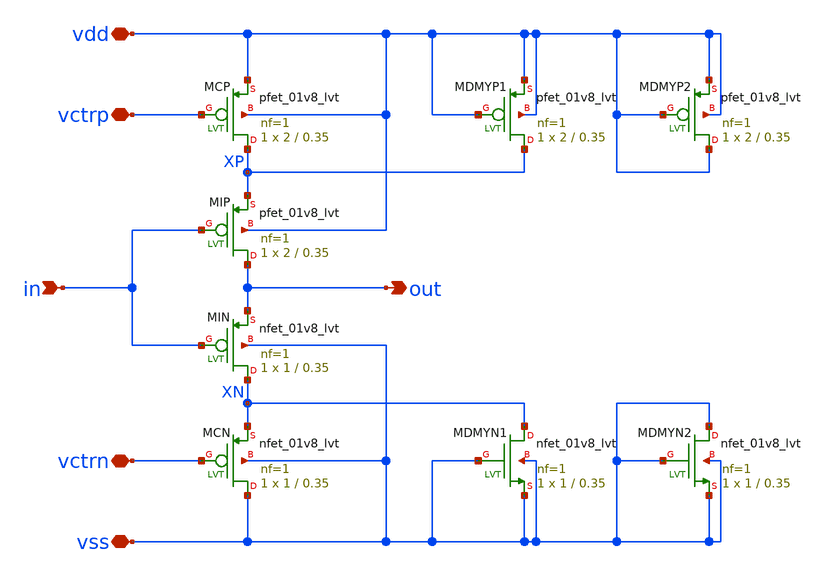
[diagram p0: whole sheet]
** sch_path: xschem/rvco_11st_curstav.sch
**.subckt rvco_11st_curstav vctrp vctrn vdd vss in out
*.iopin vctrp
*.iopin vctrn
*.iopin vdd
*.iopin vss
*.ipin in
*.opin out
XMIP out in XP vdd sky130_fd_pr__pfet_01v8_lvt L=0.35 W=2 nf=1 ad='int((1 + 1)/2) * 2 / 1 * 0.29' as='int((1 + 2)/2) * 2 / 1 * 0.29'
+ pd='2*int((1 + 1)/2) * (2 / 1 + 0.29)' ps='2*int((1 + 2)/2) * (2 / 1 + 0.29)' nrd='0.29 / 2 ' nrs='0.29 / 2 '
+ sa=0 sb=0 sd=0 mult=1 m=1
XMCP XP vctrp vdd vdd sky130_fd_pr__pfet_01v8_lvt L=0.35 W=2 nf=1 ad='int((1 + 1)/2) * 2 / 1 * 0.29'
+ as='int((1 + 2)/2) * 2 / 1 * 0.29' pd='2*int((1 + 1)/2) * (2 / 1 + 0.29)' ps='2*int((1 + 2)/2) * (2 / 1 + 0.29)'
+ nrd='0.29 / 2 ' nrs='0.29 / 2 ' sa=0 sb=0 sd=0 mult=1 m=1
XMIN XN in out vss sky130_fd_pr__nfet_01v8_lvt L=0.35 W=1 nf=1 ad='int((1 + 1)/2) * 1 / 1 * 0.29' as='int((1 + 2)/2) * 1 / 1 * 0.29'
+ pd='2*int((1 + 1)/2) * (1 / 1 + 0.29)' ps='2*int((1 + 2)/2) * (1 / 1 + 0.29)' nrd='0.29 / 1 ' nrs='0.29 / 1 '
+ sa=0 sb=0 sd=0 mult=1 m=1
XMCN vss vctrn XN vss sky130_fd_pr__nfet_01v8_lvt L=0.35 W=1 nf=1 ad='int((1 + 1)/2) * 1 / 1 * 0.29'
+ as='int((1 + 2)/2) * 1 / 1 * 0.29' pd='2*int((1 + 1)/2) * (1 / 1 + 0.29)' ps='2*int((1 + 2)/2) * (1 / 1 + 0.29)'
+ nrd='0.29 / 1 ' nrs='0.29 / 1 ' sa=0 sb=0 sd=0 mult=1 m=1
XMDMYP1 XP vdd vdd vdd sky130_fd_pr__pfet_01v8_lvt L=0.35 W=2 nf=1 ad='int((1 + 1)/2) * 2 / 1 * 0.29'
+ as='int((1 + 2)/2) * 2 / 1 * 0.29' pd='2*int((1 + 1)/2) * (2 / 1 + 0.29)' ps='2*int((1 + 2)/2) * (2 / 1 + 0.29)'
+ nrd='0.29 / 2 ' nrs='0.29 / 2 ' sa=0 sb=0 sd=0 mult=1 m=1
XMDMYP2 vdd vdd vdd vdd sky130_fd_pr__pfet_01v8_lvt L=0.35 W=2 nf=1 ad='int((1 + 1)/2) * 2 / 1 * 0.29'
+ as='int((1 + 2)/2) * 2 / 1 * 0.29' pd='2*int((1 + 1)/2) * (2 / 1 + 0.29)' ps='2*int((1 + 2)/2) * (2 / 1 + 0.29)'
+ nrd='0.29 / 2 ' nrs='0.29 / 2 ' sa=0 sb=0 sd=0 mult=1 m=1
XMDMYN1 XN vss vss vss sky130_fd_pr__nfet_01v8_lvt L=0.35 W=1 nf=1 ad='int((1 + 1)/2) * 1 / 1 * 0.29'
+ as='int((1 + 2)/2) * 1 / 1 * 0.29' pd='2*int((1 + 1)/2) * (1 / 1 + 0.29)' ps='2*int((1 + 2)/2) * (1 / 1 + 0.29)'
+ nrd='0.29 / 1 ' nrs='0.29 / 1 ' sa=0 sb=0 sd=0 mult=1 m=1
XMDMYN2 vss vss vss vss sky130_fd_pr__nfet_01v8_lvt L=0.35 W=1 nf=1 ad='int((1 + 1)/2) * 1 / 1 * 0.29'
+ as='int((1 + 2)/2) * 1 / 1 * 0.29' pd='2*int((1 + 1)/2) * (1 / 1 + 0.29)' ps='2*int((1 + 2)/2) * (1 / 1 + 0.29)'
+ nrd='0.29 / 1 ' nrs='0.29 / 1 ' sa=0 sb=0 sd=0 mult=1 m=1
**.ends
.end
